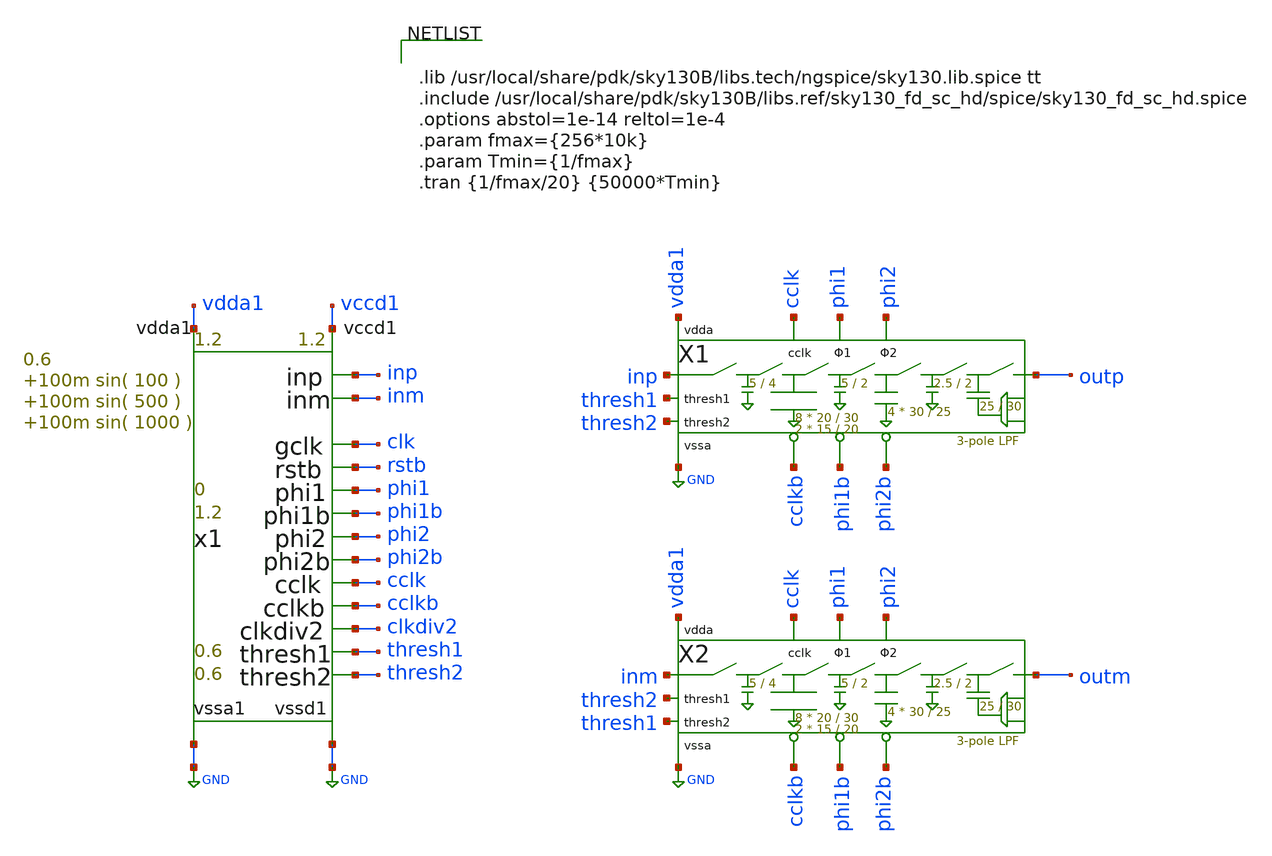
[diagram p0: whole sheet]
** sch_path: xschem/Switched_Caps/filter_tb.sch
**.subckt filter_tb
x1 thresh1 thresh2 vdda1 GND inp inm clk rstb vccd1 GND phi1 phi1b phi2 phi2b cclk cclkb clkdiv2 risc_signals
+ p_vdda1=1.2 p_vccd1=1.2 p_fclk={256*10k} p_duty_cycle=0.5 p_rstb_delay={1.5/p_fclk} p_rstb_tr=5n p_thresh1=0.6
+ p_thresh2=0.6 p_vpb=0 p_vnb=1.2 p_vcm=0.6 p_amp1=100m p_f1=100 p_amp2=100m p_f2=500 p_amp3=100m p_f3=1000
X1 inp outp phi2 phi1 phi1b phi2b cclk cclkb thresh1 thresh2 vdda1 GND filter WC1=20 LC1=30 WC1B=15
+ LC1B=20 WC2=30 LC2=25 WC3=25 LC3=30 WCS1=5 LCS1=4 WCS2=5 LCS2=2 WCS3=2.5 LCS3=2
X2 inm outm phi2 phi1 phi1b phi2b cclk cclkb thresh2 thresh1 vdda1 GND filter WC1=20 LC1=30 WC1B=15
+ LC1B=20 WC2=30 LC2=25 WC3=25 LC3=30 WCS1=5 LCS1=4 WCS2=5 LCS2=2 WCS3=2.5 LCS3=2
**** begin user architecture code


.lib /usr/local/share/pdk/sky130B/libs.tech/ngspice/sky130.lib.spice tt
.include /usr/local/share/pdk/sky130B/libs.ref/sky130_fd_sc_hd/spice/sky130_fd_sc_hd.spice
.options abstol=1e-14 reltol=1e-4
.param fmax={256*10k}
.param Tmin={1/fmax}
.tran {1/fmax/20} {50000*Tmin}


**** end user architecture code
**.ends
.GLOBAL GND
.end
